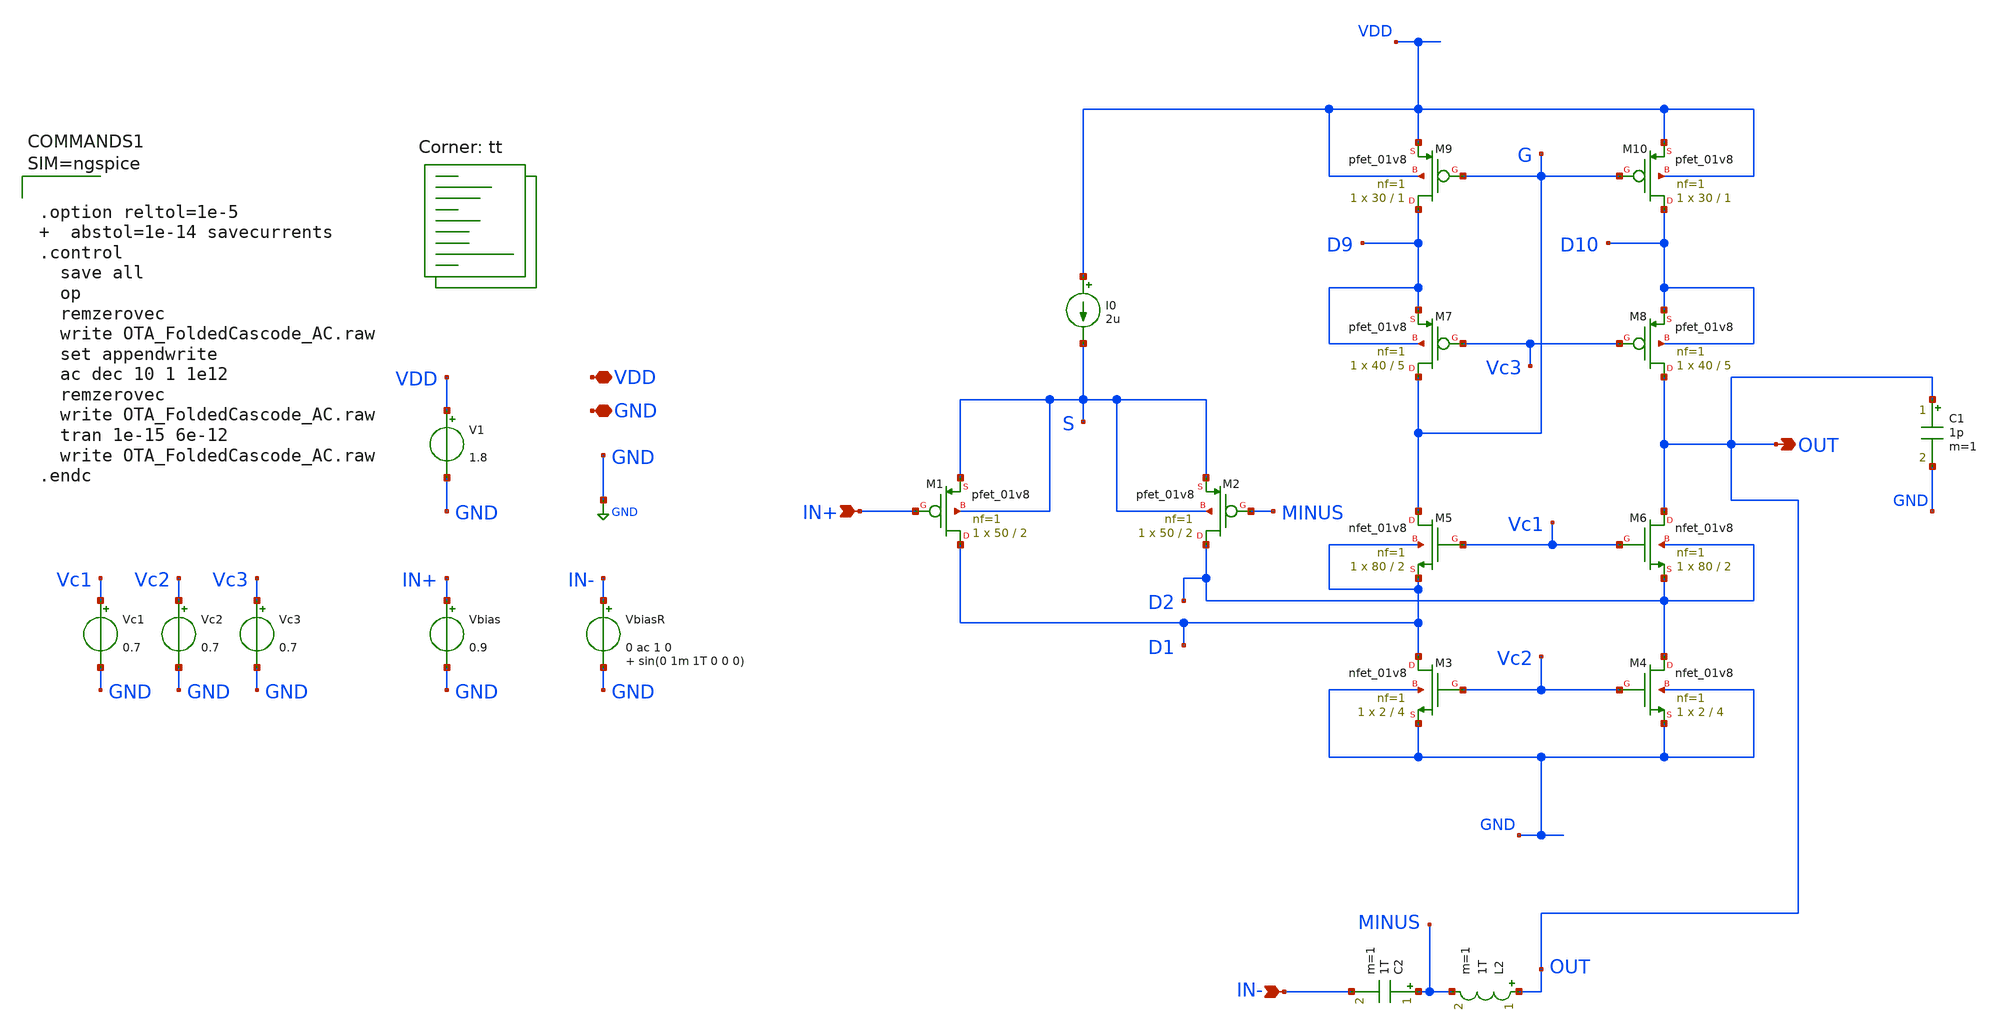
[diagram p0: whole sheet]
** sch_path: xschem/OTA_FoldedCascode_AC.sch
**.subckt OTA_FoldedCascode_AC VDD GND IN+ IN- OUT
*.iopin VDD
*.iopin GND
*.ipin IN+
*.ipin IN-
*.opin OUT
V1 VDD GND 1.8
Vbias IN+ GND 0.9
VbiasR IN- GND 0 ac 1 0 sin(0 1m 1T 0 0 0)
I0 VDD S 2u
XM1 D1 IN+ S S sky130_fd_pr__pfet_01v8 L=2 W=50 nf=1 ad='int((nf+1)/2) * W/nf * 0.29' as='int((nf+2)/2) * W/nf * 0.29'
+ pd='2*int((nf+1)/2) * (W/nf + 0.29)' ps='2*int((nf+2)/2) * (W/nf + 0.29)' nrd='0.29 / W' nrs='0.29 / W'
+ sa=0 sb=0 sd=0 mult=1 m=1
XM2 D2 MINUS S S sky130_fd_pr__pfet_01v8 L=2 W=50 nf=1 ad='int((nf+1)/2) * W/nf * 0.29' as='int((nf+2)/2) * W/nf * 0.29'
+ pd='2*int((nf+1)/2) * (W/nf + 0.29)' ps='2*int((nf+2)/2) * (W/nf + 0.29)' nrd='0.29 / W' nrs='0.29 / W'
+ sa=0 sb=0 sd=0 mult=1 m=1
XM3 D1 Vc2 GND GND sky130_fd_pr__nfet_01v8 L=4 W=2 nf=1 ad='int((nf+1)/2) * W/nf * 0.29' as='int((nf+2)/2) * W/nf * 0.29'
+ pd='2*int((nf+1)/2) * (W/nf + 0.29)' ps='2*int((nf+2)/2) * (W/nf + 0.29)' nrd='0.29 / W' nrs='0.29 / W'
+ sa=0 sb=0 sd=0 mult=1 m=1
XM4 D2 Vc2 GND GND sky130_fd_pr__nfet_01v8 L=4 W=2 nf=1 ad='int((nf+1)/2) * W/nf * 0.29' as='int((nf+2)/2) * W/nf * 0.29'
+ pd='2*int((nf+1)/2) * (W/nf + 0.29)' ps='2*int((nf+2)/2) * (W/nf + 0.29)' nrd='0.29 / W' nrs='0.29 / W'
+ sa=0 sb=0 sd=0 mult=1 m=1
XM5 G Vc1 D1 D1 sky130_fd_pr__nfet_01v8 L=2 W=80 nf=1 ad='int((nf+1)/2) * W/nf * 0.29' as='int((nf+2)/2) * W/nf * 0.29'
+ pd='2*int((nf+1)/2) * (W/nf + 0.29)' ps='2*int((nf+2)/2) * (W/nf + 0.29)' nrd='0.29 / W' nrs='0.29 / W'
+ sa=0 sb=0 sd=0 mult=1 m=1
XM6 OUT Vc1 D2 D2 sky130_fd_pr__nfet_01v8 L=2 W=80 nf=1 ad='int((nf+1)/2) * W/nf * 0.29' as='int((nf+2)/2) * W/nf * 0.29'
+ pd='2*int((nf+1)/2) * (W/nf + 0.29)' ps='2*int((nf+2)/2) * (W/nf + 0.29)' nrd='0.29 / W' nrs='0.29 / W'
+ sa=0 sb=0 sd=0 mult=1 m=1
XM7 G Vc3 D9 D9 sky130_fd_pr__pfet_01v8 L=5 W=40 nf=1 ad='int((nf+1)/2) * W/nf * 0.29' as='int((nf+2)/2) * W/nf * 0.29'
+ pd='2*int((nf+1)/2) * (W/nf + 0.29)' ps='2*int((nf+2)/2) * (W/nf + 0.29)' nrd='0.29 / W' nrs='0.29 / W'
+ sa=0 sb=0 sd=0 mult=1 m=1
XM8 OUT Vc3 D10 D10 sky130_fd_pr__pfet_01v8 L=5 W=40 nf=1 ad='int((nf+1)/2) * W/nf * 0.29' as='int((nf+2)/2) * W/nf * 0.29'
+ pd='2*int((nf+1)/2) * (W/nf + 0.29)' ps='2*int((nf+2)/2) * (W/nf + 0.29)' nrd='0.29 / W' nrs='0.29 / W'
+ sa=0 sb=0 sd=0 mult=1 m=1
XM9 D9 G VDD VDD sky130_fd_pr__pfet_01v8 L=1 W=30 nf=1 ad='int((nf+1)/2) * W/nf * 0.29' as='int((nf+2)/2) * W/nf * 0.29'
+ pd='2*int((nf+1)/2) * (W/nf + 0.29)' ps='2*int((nf+2)/2) * (W/nf + 0.29)' nrd='0.29 / W' nrs='0.29 / W'
+ sa=0 sb=0 sd=0 mult=1 m=1
XM10 D10 G VDD VDD sky130_fd_pr__pfet_01v8 L=1 W=30 nf=1 ad='int((nf+1)/2) * W/nf * 0.29' as='int((nf+2)/2) * W/nf * 0.29'
+ pd='2*int((nf+1)/2) * (W/nf + 0.29)' ps='2*int((nf+2)/2) * (W/nf + 0.29)' nrd='0.29 / W' nrs='0.29 / W'
+ sa=0 sb=0 sd=0 mult=1 m=1
Vc1 Vc1 GND 0.7
Vc2 Vc2 GND 0.7
Vc3 Vc3 GND 0.7
C2 MINUS IN- 1T m=1
L2 OUT MINUS 1T m=1
C1 OUT GND 1p m=1
**** begin user architecture code



.option reltol=1e-5   abstol=1e-14 savecurrents
.control
  save all
  op
  remzerovec
  write OTA_FoldedCascode_AC.raw
  set appendwrite
  ac dec 10 1 1e12
  remzerovec
  write OTA_FoldedCascode_AC.raw
  tran 1e-15 6e-12
  write OTA_FoldedCascode_AC.raw
.endc



.lib $::SKYWATER_MODELS/sky130.lib.spice tt
**** end user architecture code
**.ends
.GLOBAL GND
.end
